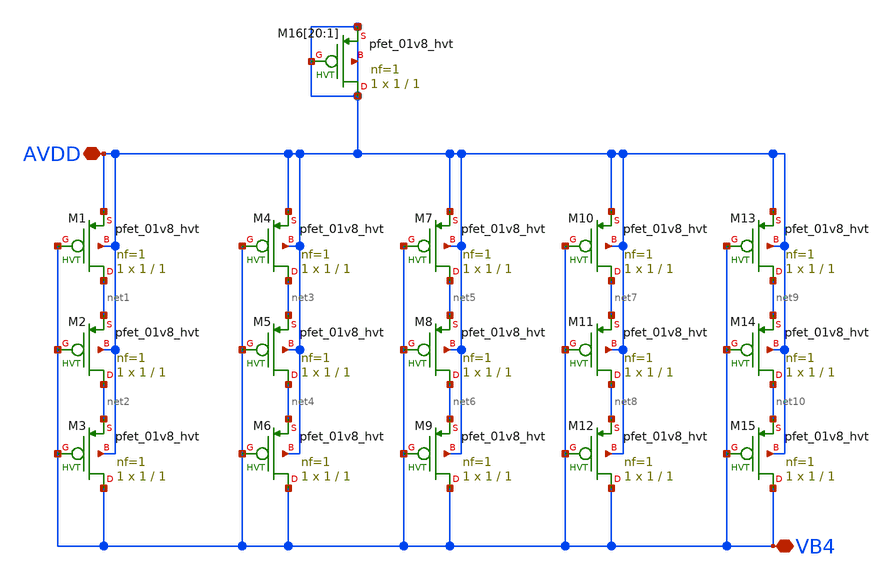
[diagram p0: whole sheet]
** sch_path: xschem/INA_layout_v2/bias/pbias_vb4.sch
**.subckt pbias_vb4 VB4 AVDD
*.iopin VB4
*.iopin AVDD
XM1 net1 VB4 AVDD AVDD sky130_fd_pr__pfet_01v8_hvt L=1 W=1 nf=1 ad='int((nf+1)/2) * W/nf * 0.29' as='int((nf+2)/2) * W/nf * 0.29'
+ pd='2*int((nf+1)/2) * (W/nf + 0.29)' ps='2*int((nf+2)/2) * (W/nf + 0.29)' nrd='0.29 / W' nrs='0.29 / W'
+ sa=0 sb=0 sd=0 mult=1 m=1
XM2 net2 VB4 net1 AVDD sky130_fd_pr__pfet_01v8_hvt L=1 W=1 nf=1 ad='int((nf+1)/2) * W/nf * 0.29' as='int((nf+2)/2) * W/nf * 0.29'
+ pd='2*int((nf+1)/2) * (W/nf + 0.29)' ps='2*int((nf+2)/2) * (W/nf + 0.29)' nrd='0.29 / W' nrs='0.29 / W'
+ sa=0 sb=0 sd=0 mult=1 m=1
XM3 VB4 VB4 net2 AVDD sky130_fd_pr__pfet_01v8_hvt L=1 W=1 nf=1 ad='int((nf+1)/2) * W/nf * 0.29' as='int((nf+2)/2) * W/nf * 0.29'
+ pd='2*int((nf+1)/2) * (W/nf + 0.29)' ps='2*int((nf+2)/2) * (W/nf + 0.29)' nrd='0.29 / W' nrs='0.29 / W'
+ sa=0 sb=0 sd=0 mult=1 m=1
XM4 net3 VB4 AVDD AVDD sky130_fd_pr__pfet_01v8_hvt L=1 W=1 nf=1 ad='int((nf+1)/2) * W/nf * 0.29' as='int((nf+2)/2) * W/nf * 0.29'
+ pd='2*int((nf+1)/2) * (W/nf + 0.29)' ps='2*int((nf+2)/2) * (W/nf + 0.29)' nrd='0.29 / W' nrs='0.29 / W'
+ sa=0 sb=0 sd=0 mult=1 m=1
XM5 net4 VB4 net3 AVDD sky130_fd_pr__pfet_01v8_hvt L=1 W=1 nf=1 ad='int((nf+1)/2) * W/nf * 0.29' as='int((nf+2)/2) * W/nf * 0.29'
+ pd='2*int((nf+1)/2) * (W/nf + 0.29)' ps='2*int((nf+2)/2) * (W/nf + 0.29)' nrd='0.29 / W' nrs='0.29 / W'
+ sa=0 sb=0 sd=0 mult=1 m=1
XM6 VB4 VB4 net4 AVDD sky130_fd_pr__pfet_01v8_hvt L=1 W=1 nf=1 ad='int((nf+1)/2) * W/nf * 0.29' as='int((nf+2)/2) * W/nf * 0.29'
+ pd='2*int((nf+1)/2) * (W/nf + 0.29)' ps='2*int((nf+2)/2) * (W/nf + 0.29)' nrd='0.29 / W' nrs='0.29 / W'
+ sa=0 sb=0 sd=0 mult=1 m=1
XM7 net5 VB4 AVDD AVDD sky130_fd_pr__pfet_01v8_hvt L=1 W=1 nf=1 ad='int((nf+1)/2) * W/nf * 0.29' as='int((nf+2)/2) * W/nf * 0.29'
+ pd='2*int((nf+1)/2) * (W/nf + 0.29)' ps='2*int((nf+2)/2) * (W/nf + 0.29)' nrd='0.29 / W' nrs='0.29 / W'
+ sa=0 sb=0 sd=0 mult=1 m=1
XM8 net6 VB4 net5 AVDD sky130_fd_pr__pfet_01v8_hvt L=1 W=1 nf=1 ad='int((nf+1)/2) * W/nf * 0.29' as='int((nf+2)/2) * W/nf * 0.29'
+ pd='2*int((nf+1)/2) * (W/nf + 0.29)' ps='2*int((nf+2)/2) * (W/nf + 0.29)' nrd='0.29 / W' nrs='0.29 / W'
+ sa=0 sb=0 sd=0 mult=1 m=1
XM9 VB4 VB4 net6 AVDD sky130_fd_pr__pfet_01v8_hvt L=1 W=1 nf=1 ad='int((nf+1)/2) * W/nf * 0.29' as='int((nf+2)/2) * W/nf * 0.29'
+ pd='2*int((nf+1)/2) * (W/nf + 0.29)' ps='2*int((nf+2)/2) * (W/nf + 0.29)' nrd='0.29 / W' nrs='0.29 / W'
+ sa=0 sb=0 sd=0 mult=1 m=1
XM10 net7 VB4 AVDD AVDD sky130_fd_pr__pfet_01v8_hvt L=1 W=1 nf=1 ad='int((nf+1)/2) * W/nf * 0.29' as='int((nf+2)/2) * W/nf * 0.29'
+ pd='2*int((nf+1)/2) * (W/nf + 0.29)' ps='2*int((nf+2)/2) * (W/nf + 0.29)' nrd='0.29 / W' nrs='0.29 / W'
+ sa=0 sb=0 sd=0 mult=1 m=1
XM11 net8 VB4 net7 AVDD sky130_fd_pr__pfet_01v8_hvt L=1 W=1 nf=1 ad='int((nf+1)/2) * W/nf * 0.29' as='int((nf+2)/2) * W/nf * 0.29'
+ pd='2*int((nf+1)/2) * (W/nf + 0.29)' ps='2*int((nf+2)/2) * (W/nf + 0.29)' nrd='0.29 / W' nrs='0.29 / W'
+ sa=0 sb=0 sd=0 mult=1 m=1
XM12 VB4 VB4 net8 AVDD sky130_fd_pr__pfet_01v8_hvt L=1 W=1 nf=1 ad='int((nf+1)/2) * W/nf * 0.29' as='int((nf+2)/2) * W/nf * 0.29'
+ pd='2*int((nf+1)/2) * (W/nf + 0.29)' ps='2*int((nf+2)/2) * (W/nf + 0.29)' nrd='0.29 / W' nrs='0.29 / W'
+ sa=0 sb=0 sd=0 mult=1 m=1
XM13 net9 VB4 AVDD AVDD sky130_fd_pr__pfet_01v8_hvt L=1 W=1 nf=1 ad='int((nf+1)/2) * W/nf * 0.29' as='int((nf+2)/2) * W/nf * 0.29'
+ pd='2*int((nf+1)/2) * (W/nf + 0.29)' ps='2*int((nf+2)/2) * (W/nf + 0.29)' nrd='0.29 / W' nrs='0.29 / W'
+ sa=0 sb=0 sd=0 mult=1 m=1
XM14 net10 VB4 net9 AVDD sky130_fd_pr__pfet_01v8_hvt L=1 W=1 nf=1 ad='int((nf+1)/2) * W/nf * 0.29' as='int((nf+2)/2) * W/nf * 0.29'
+ pd='2*int((nf+1)/2) * (W/nf + 0.29)' ps='2*int((nf+2)/2) * (W/nf + 0.29)' nrd='0.29 / W' nrs='0.29 / W'
+ sa=0 sb=0 sd=0 mult=1 m=1
XM15 VB4 VB4 net10 AVDD sky130_fd_pr__pfet_01v8_hvt L=1 W=1 nf=1 ad='int((nf+1)/2) * W/nf * 0.29' as='int((nf+2)/2) * W/nf * 0.29'
+ pd='2*int((nf+1)/2) * (W/nf + 0.29)' ps='2*int((nf+2)/2) * (W/nf + 0.29)' nrd='0.29 / W' nrs='0.29 / W'
+ sa=0 sb=0 sd=0 mult=1 m=1
XM16[20] AVDD AVDD AVDD AVDD sky130_fd_pr__pfet_01v8_hvt L=1 W=1 nf=1 ad='int((nf+1)/2) * W/nf * 0.29'
+ as='int((nf+2)/2) * W/nf * 0.29' pd='2*int((nf+1)/2) * (W/nf + 0.29)' ps='2*int((nf+2)/2) * (W/nf + 0.29)'
+ nrd='0.29 / W' nrs='0.29 / W' sa=0 sb=0 sd=0 mult=1 m=1
XM16[19] AVDD AVDD AVDD AVDD sky130_fd_pr__pfet_01v8_hvt L=1 W=1 nf=1 ad='int((nf+1)/2) * W/nf * 0.29'
+ as='int((nf+2)/2) * W/nf * 0.29' pd='2*int((nf+1)/2) * (W/nf + 0.29)' ps='2*int((nf+2)/2) * (W/nf + 0.29)'
+ nrd='0.29 / W' nrs='0.29 / W' sa=0 sb=0 sd=0 mult=1 m=1
XM16[18] AVDD AVDD AVDD AVDD sky130_fd_pr__pfet_01v8_hvt L=1 W=1 nf=1 ad='int((nf+1)/2) * W/nf * 0.29'
+ as='int((nf+2)/2) * W/nf * 0.29' pd='2*int((nf+1)/2) * (W/nf + 0.29)' ps='2*int((nf+2)/2) * (W/nf + 0.29)'
+ nrd='0.29 / W' nrs='0.29 / W' sa=0 sb=0 sd=0 mult=1 m=1
XM16[17] AVDD AVDD AVDD AVDD sky130_fd_pr__pfet_01v8_hvt L=1 W=1 nf=1 ad='int((nf+1)/2) * W/nf * 0.29'
+ as='int((nf+2)/2) * W/nf * 0.29' pd='2*int((nf+1)/2) * (W/nf + 0.29)' ps='2*int((nf+2)/2) * (W/nf + 0.29)'
+ nrd='0.29 / W' nrs='0.29 / W' sa=0 sb=0 sd=0 mult=1 m=1
XM16[16] AVDD AVDD AVDD AVDD sky130_fd_pr__pfet_01v8_hvt L=1 W=1 nf=1 ad='int((nf+1)/2) * W/nf * 0.29'
+ as='int((nf+2)/2) * W/nf * 0.29' pd='2*int((nf+1)/2) * (W/nf + 0.29)' ps='2*int((nf+2)/2) * (W/nf + 0.29)'
+ nrd='0.29 / W' nrs='0.29 / W' sa=0 sb=0 sd=0 mult=1 m=1
XM16[15] AVDD AVDD AVDD AVDD sky130_fd_pr__pfet_01v8_hvt L=1 W=1 nf=1 ad='int((nf+1)/2) * W/nf * 0.29'
+ as='int((nf+2)/2) * W/nf * 0.29' pd='2*int((nf+1)/2) * (W/nf + 0.29)' ps='2*int((nf+2)/2) * (W/nf + 0.29)'
+ nrd='0.29 / W' nrs='0.29 / W' sa=0 sb=0 sd=0 mult=1 m=1
XM16[14] AVDD AVDD AVDD AVDD sky130_fd_pr__pfet_01v8_hvt L=1 W=1 nf=1 ad='int((nf+1)/2) * W/nf * 0.29'
+ as='int((nf+2)/2) * W/nf * 0.29' pd='2*int((nf+1)/2) * (W/nf + 0.29)' ps='2*int((nf+2)/2) * (W/nf + 0.29)'
+ nrd='0.29 / W' nrs='0.29 / W' sa=0 sb=0 sd=0 mult=1 m=1
XM16[13] AVDD AVDD AVDD AVDD sky130_fd_pr__pfet_01v8_hvt L=1 W=1 nf=1 ad='int((nf+1)/2) * W/nf * 0.29'
+ as='int((nf+2)/2) * W/nf * 0.29' pd='2*int((nf+1)/2) * (W/nf + 0.29)' ps='2*int((nf+2)/2) * (W/nf + 0.29)'
+ nrd='0.29 / W' nrs='0.29 / W' sa=0 sb=0 sd=0 mult=1 m=1
XM16[12] AVDD AVDD AVDD AVDD sky130_fd_pr__pfet_01v8_hvt L=1 W=1 nf=1 ad='int((nf+1)/2) * W/nf * 0.29'
+ as='int((nf+2)/2) * W/nf * 0.29' pd='2*int((nf+1)/2) * (W/nf + 0.29)' ps='2*int((nf+2)/2) * (W/nf + 0.29)'
+ nrd='0.29 / W' nrs='0.29 / W' sa=0 sb=0 sd=0 mult=1 m=1
XM16[11] AVDD AVDD AVDD AVDD sky130_fd_pr__pfet_01v8_hvt L=1 W=1 nf=1 ad='int((nf+1)/2) * W/nf * 0.29'
+ as='int((nf+2)/2) * W/nf * 0.29' pd='2*int((nf+1)/2) * (W/nf + 0.29)' ps='2*int((nf+2)/2) * (W/nf + 0.29)'
+ nrd='0.29 / W' nrs='0.29 / W' sa=0 sb=0 sd=0 mult=1 m=1
XM16[10] AVDD AVDD AVDD AVDD sky130_fd_pr__pfet_01v8_hvt L=1 W=1 nf=1 ad='int((nf+1)/2) * W/nf * 0.29'
+ as='int((nf+2)/2) * W/nf * 0.29' pd='2*int((nf+1)/2) * (W/nf + 0.29)' ps='2*int((nf+2)/2) * (W/nf + 0.29)'
+ nrd='0.29 / W' nrs='0.29 / W' sa=0 sb=0 sd=0 mult=1 m=1
XM16[9] AVDD AVDD AVDD AVDD sky130_fd_pr__pfet_01v8_hvt L=1 W=1 nf=1 ad='int((nf+1)/2) * W/nf * 0.29'
+ as='int((nf+2)/2) * W/nf * 0.29' pd='2*int((nf+1)/2) * (W/nf + 0.29)' ps='2*int((nf+2)/2) * (W/nf + 0.29)'
+ nrd='0.29 / W' nrs='0.29 / W' sa=0 sb=0 sd=0 mult=1 m=1
XM16[8] AVDD AVDD AVDD AVDD sky130_fd_pr__pfet_01v8_hvt L=1 W=1 nf=1 ad='int((nf+1)/2) * W/nf * 0.29'
+ as='int((nf+2)/2) * W/nf * 0.29' pd='2*int((nf+1)/2) * (W/nf + 0.29)' ps='2*int((nf+2)/2) * (W/nf + 0.29)'
+ nrd='0.29 / W' nrs='0.29 / W' sa=0 sb=0 sd=0 mult=1 m=1
XM16[7] AVDD AVDD AVDD AVDD sky130_fd_pr__pfet_01v8_hvt L=1 W=1 nf=1 ad='int((nf+1)/2) * W/nf * 0.29'
+ as='int((nf+2)/2) * W/nf * 0.29' pd='2*int((nf+1)/2) * (W/nf + 0.29)' ps='2*int((nf+2)/2) * (W/nf + 0.29)'
+ nrd='0.29 / W' nrs='0.29 / W' sa=0 sb=0 sd=0 mult=1 m=1
XM16[6] AVDD AVDD AVDD AVDD sky130_fd_pr__pfet_01v8_hvt L=1 W=1 nf=1 ad='int((nf+1)/2) * W/nf * 0.29'
+ as='int((nf+2)/2) * W/nf * 0.29' pd='2*int((nf+1)/2) * (W/nf + 0.29)' ps='2*int((nf+2)/2) * (W/nf + 0.29)'
+ nrd='0.29 / W' nrs='0.29 / W' sa=0 sb=0 sd=0 mult=1 m=1
XM16[5] AVDD AVDD AVDD AVDD sky130_fd_pr__pfet_01v8_hvt L=1 W=1 nf=1 ad='int((nf+1)/2) * W/nf * 0.29'
+ as='int((nf+2)/2) * W/nf * 0.29' pd='2*int((nf+1)/2) * (W/nf + 0.29)' ps='2*int((nf+2)/2) * (W/nf + 0.29)'
+ nrd='0.29 / W' nrs='0.29 / W' sa=0 sb=0 sd=0 mult=1 m=1
XM16[4] AVDD AVDD AVDD AVDD sky130_fd_pr__pfet_01v8_hvt L=1 W=1 nf=1 ad='int((nf+1)/2) * W/nf * 0.29'
+ as='int((nf+2)/2) * W/nf * 0.29' pd='2*int((nf+1)/2) * (W/nf + 0.29)' ps='2*int((nf+2)/2) * (W/nf + 0.29)'
+ nrd='0.29 / W' nrs='0.29 / W' sa=0 sb=0 sd=0 mult=1 m=1
XM16[3] AVDD AVDD AVDD AVDD sky130_fd_pr__pfet_01v8_hvt L=1 W=1 nf=1 ad='int((nf+1)/2) * W/nf * 0.29'
+ as='int((nf+2)/2) * W/nf * 0.29' pd='2*int((nf+1)/2) * (W/nf + 0.29)' ps='2*int((nf+2)/2) * (W/nf + 0.29)'
+ nrd='0.29 / W' nrs='0.29 / W' sa=0 sb=0 sd=0 mult=1 m=1
XM16[2] AVDD AVDD AVDD AVDD sky130_fd_pr__pfet_01v8_hvt L=1 W=1 nf=1 ad='int((nf+1)/2) * W/nf * 0.29'
+ as='int((nf+2)/2) * W/nf * 0.29' pd='2*int((nf+1)/2) * (W/nf + 0.29)' ps='2*int((nf+2)/2) * (W/nf + 0.29)'
+ nrd='0.29 / W' nrs='0.29 / W' sa=0 sb=0 sd=0 mult=1 m=1
XM16[1] AVDD AVDD AVDD AVDD sky130_fd_pr__pfet_01v8_hvt L=1 W=1 nf=1 ad='int((nf+1)/2) * W/nf * 0.29'
+ as='int((nf+2)/2) * W/nf * 0.29' pd='2*int((nf+1)/2) * (W/nf + 0.29)' ps='2*int((nf+2)/2) * (W/nf + 0.29)'
+ nrd='0.29 / W' nrs='0.29 / W' sa=0 sb=0 sd=0 mult=1 m=1
**.ends
.end
